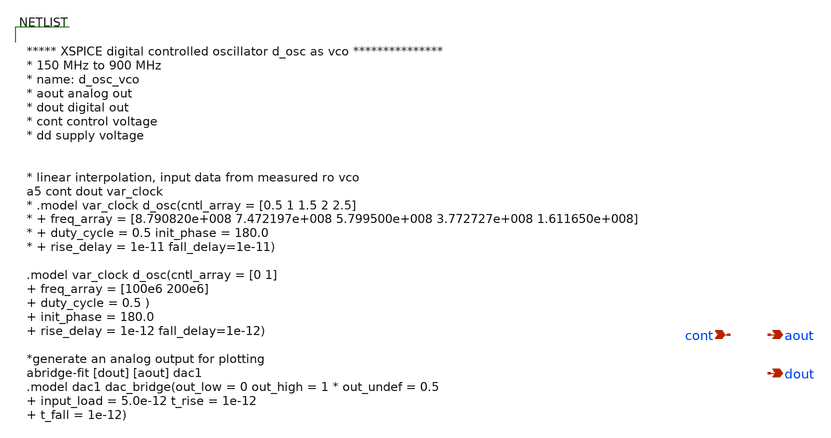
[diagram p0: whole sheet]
** sch_path: designs/libs/model_pll/dvco_model.sch
**.subckt dvco_model cont aout dout
*.ipin cont
*.opin aout
*.opin dout
**** begin user architecture code


***** XSPICE digital controlled oscillator d_osc as vco ***************
* 150 MHz to 900 MHz
* name: d_osc_vco
* aout analog out
* dout digital out
* cont control voltage
* dd supply voltage


* linear interpolation, input data from measured ro vco
a5 cont dout var_clock
* .model var_clock d_osc(cntl_array = [0.5 1 1.5 2 2.5]
* + freq_array = [8.790820e+008 7.472197e+008 5.799500e+008 3.772727e+008 1.611650e+008]
* + duty_cycle = 0.5 init_phase = 180.0
* + rise_delay = 1e-11 fall_delay=1e-11)

.model var_clock d_osc(cntl_array = [0 1]  freq_array = [100e6 200e6]  duty_cycle = 0.5 )
+  init_phase = 180.0  rise_delay = 1e-12 fall_delay=1e-12)

*generate an analog output for plotting
abridge-fit [dout] [aout] dac1
.model dac1 dac_bridge(out_low = 0 out_high = 1 * out_undef = 0.5  input_load = 5.0e-12 t_rise =
+ 1e-12  t_fall = 1e-12)



**** end user architecture code
**.ends
.end
